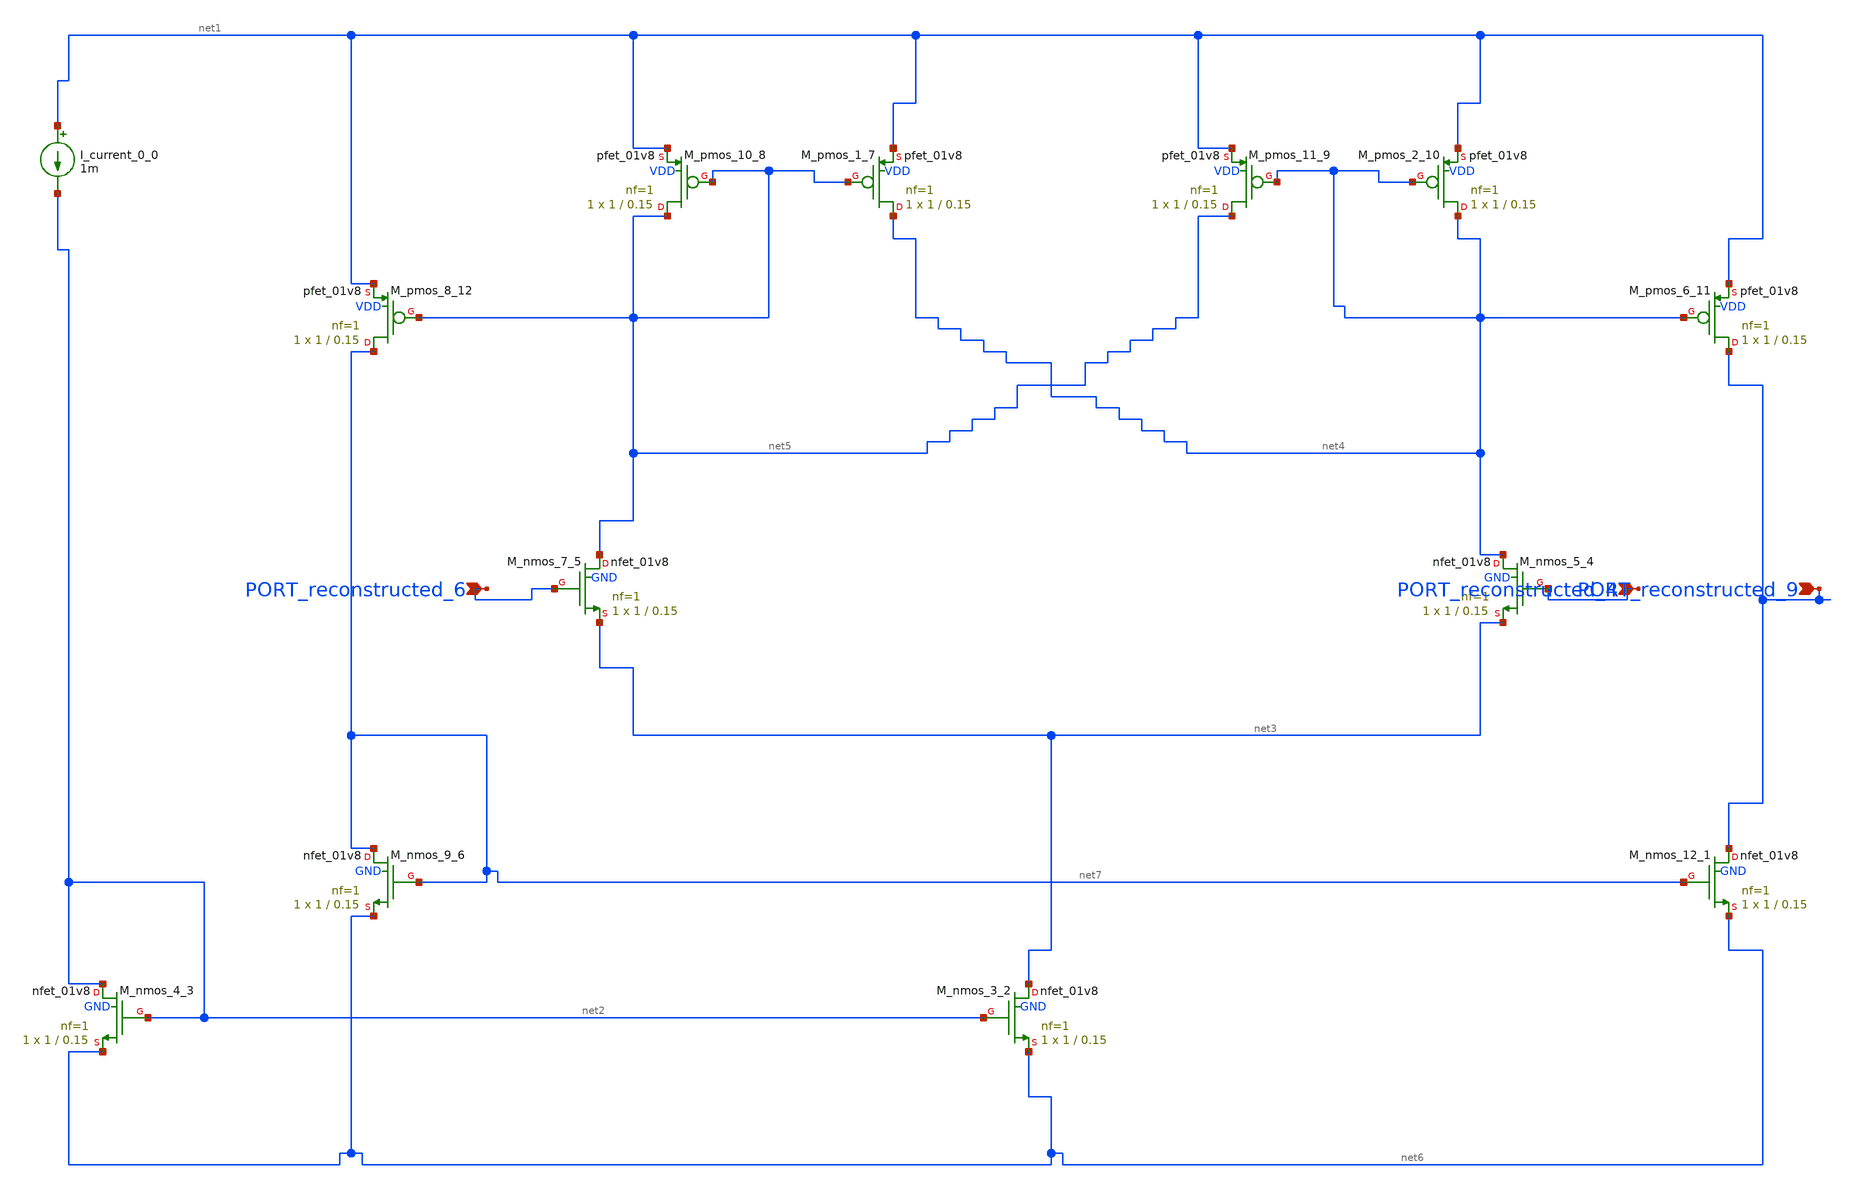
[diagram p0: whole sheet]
** sch_path: schematics/Image2Net/126.sch
**.subckt 126 PORT_reconstructed_4 PORT_reconstructed_9 PORT_reconstructed_6
*.ipin PORT_reconstructed_4
*.ipin PORT_reconstructed_9
*.ipin PORT_reconstructed_6
I_current_0_0 net1 net2 1m
XM_nmos_12_1 PORT_reconstructed_9 net7 net6 GND sky130_fd_pr__nfet_01v8 L=0.15 W=1 nf=1 ad='int((1 + 1)/2) * 1 / 1 * 0.29'
+ as='int((1 + 2)/2) * 1 / 1 * 0.29' pd='2*int((1 + 1)/2) * (1 / 1 + 0.29)' ps='2*int((1 + 2)/2) * (1 / 1 + 0.29)'
+ nrd='0.29 / 1 ' nrs='0.29 / 1 ' sa=0 sb=0 sd=0 mult=1 m=1
XM_nmos_3_2 net3 net2 net6 GND sky130_fd_pr__nfet_01v8 L=0.15 W=1 nf=1 ad='int((1 + 1)/2) * 1 / 1 * 0.29'
+ as='int((1 + 2)/2) * 1 / 1 * 0.29' pd='2*int((1 + 1)/2) * (1 / 1 + 0.29)' ps='2*int((1 + 2)/2) * (1 / 1 + 0.29)'
+ nrd='0.29 / 1 ' nrs='0.29 / 1 ' sa=0 sb=0 sd=0 mult=1 m=1
XM_nmos_4_3 net2 net2 net6 GND sky130_fd_pr__nfet_01v8 L=0.15 W=1 nf=1 ad='int((1 + 1)/2) * 1 / 1 * 0.29'
+ as='int((1 + 2)/2) * 1 / 1 * 0.29' pd='2*int((1 + 1)/2) * (1 / 1 + 0.29)' ps='2*int((1 + 2)/2) * (1 / 1 + 0.29)'
+ nrd='0.29 / 1 ' nrs='0.29 / 1 ' sa=0 sb=0 sd=0 mult=1 m=1
XM_nmos_5_4 net4 PORT_reconstructed_4 net3 GND sky130_fd_pr__nfet_01v8 L=0.15 W=1 nf=1 ad='int((1 + 1)/2) * 1 / 1 * 0.29'
+ as='int((1 + 2)/2) * 1 / 1 * 0.29' pd='2*int((1 + 1)/2) * (1 / 1 + 0.29)' ps='2*int((1 + 2)/2) * (1 / 1 + 0.29)'
+ nrd='0.29 / 1 ' nrs='0.29 / 1 ' sa=0 sb=0 sd=0 mult=1 m=1
XM_nmos_7_5 net5 PORT_reconstructed_6 net3 GND sky130_fd_pr__nfet_01v8 L=0.15 W=1 nf=1 ad='int((1 + 1)/2) * 1 / 1 * 0.29'
+ as='int((1 + 2)/2) * 1 / 1 * 0.29' pd='2*int((1 + 1)/2) * (1 / 1 + 0.29)' ps='2*int((1 + 2)/2) * (1 / 1 + 0.29)'
+ nrd='0.29 / 1 ' nrs='0.29 / 1 ' sa=0 sb=0 sd=0 mult=1 m=1
XM_nmos_9_6 net7 net7 net6 GND sky130_fd_pr__nfet_01v8 L=0.15 W=1 nf=1 ad='int((1 + 1)/2) * 1 / 1 * 0.29'
+ as='int((1 + 2)/2) * 1 / 1 * 0.29' pd='2*int((1 + 1)/2) * (1 / 1 + 0.29)' ps='2*int((1 + 2)/2) * (1 / 1 + 0.29)'
+ nrd='0.29 / 1 ' nrs='0.29 / 1 ' sa=0 sb=0 sd=0 mult=1 m=1
XM_pmos_1_7 net4 net5 net1 VDD sky130_fd_pr__pfet_01v8 L=0.15 W=1 nf=1 ad='int((1 + 1)/2) * 1 / 1 * 0.29'
+ as='int((1 + 2)/2) * 1 / 1 * 0.29' pd='2*int((1 + 1)/2) * (1 / 1 + 0.29)' ps='2*int((1 + 2)/2) * (1 / 1 + 0.29)'
+ nrd='0.29 / 1 ' nrs='0.29 / 1 ' sa=0 sb=0 sd=0 mult=1 m=1
XM_pmos_10_8 net5 net5 net1 VDD sky130_fd_pr__pfet_01v8 L=0.15 W=1 nf=1 ad='int((1 + 1)/2) * 1 / 1 * 0.29'
+ as='int((1 + 2)/2) * 1 / 1 * 0.29' pd='2*int((1 + 1)/2) * (1 / 1 + 0.29)' ps='2*int((1 + 2)/2) * (1 / 1 + 0.29)'
+ nrd='0.29 / 1 ' nrs='0.29 / 1 ' sa=0 sb=0 sd=0 mult=1 m=1
XM_pmos_11_9 net5 net4 net1 VDD sky130_fd_pr__pfet_01v8 L=0.15 W=1 nf=1 ad='int((1 + 1)/2) * 1 / 1 * 0.29'
+ as='int((1 + 2)/2) * 1 / 1 * 0.29' pd='2*int((1 + 1)/2) * (1 / 1 + 0.29)' ps='2*int((1 + 2)/2) * (1 / 1 + 0.29)'
+ nrd='0.29 / 1 ' nrs='0.29 / 1 ' sa=0 sb=0 sd=0 mult=1 m=1
XM_pmos_2_10 net4 net4 net1 VDD sky130_fd_pr__pfet_01v8 L=0.15 W=1 nf=1 ad='int((1 + 1)/2) * 1 / 1 * 0.29'
+ as='int((1 + 2)/2) * 1 / 1 * 0.29' pd='2*int((1 + 1)/2) * (1 / 1 + 0.29)' ps='2*int((1 + 2)/2) * (1 / 1 + 0.29)'
+ nrd='0.29 / 1 ' nrs='0.29 / 1 ' sa=0 sb=0 sd=0 mult=1 m=1
XM_pmos_6_11 PORT_reconstructed_9 net4 net1 VDD sky130_fd_pr__pfet_01v8 L=0.15 W=1 nf=1 ad='int((1 + 1)/2) * 1 / 1 * 0.29'
+ as='int((1 + 2)/2) * 1 / 1 * 0.29' pd='2*int((1 + 1)/2) * (1 / 1 + 0.29)' ps='2*int((1 + 2)/2) * (1 / 1 + 0.29)'
+ nrd='0.29 / 1 ' nrs='0.29 / 1 ' sa=0 sb=0 sd=0 mult=1 m=1
XM_pmos_8_12 net7 net5 net1 VDD sky130_fd_pr__pfet_01v8 L=0.15 W=1 nf=1 ad='int((1 + 1)/2) * 1 / 1 * 0.29'
+ as='int((1 + 2)/2) * 1 / 1 * 0.29' pd='2*int((1 + 1)/2) * (1 / 1 + 0.29)' ps='2*int((1 + 2)/2) * (1 / 1 + 0.29)'
+ nrd='0.29 / 1 ' nrs='0.29 / 1 ' sa=0 sb=0 sd=0 mult=1 m=1
**.ends
.end
